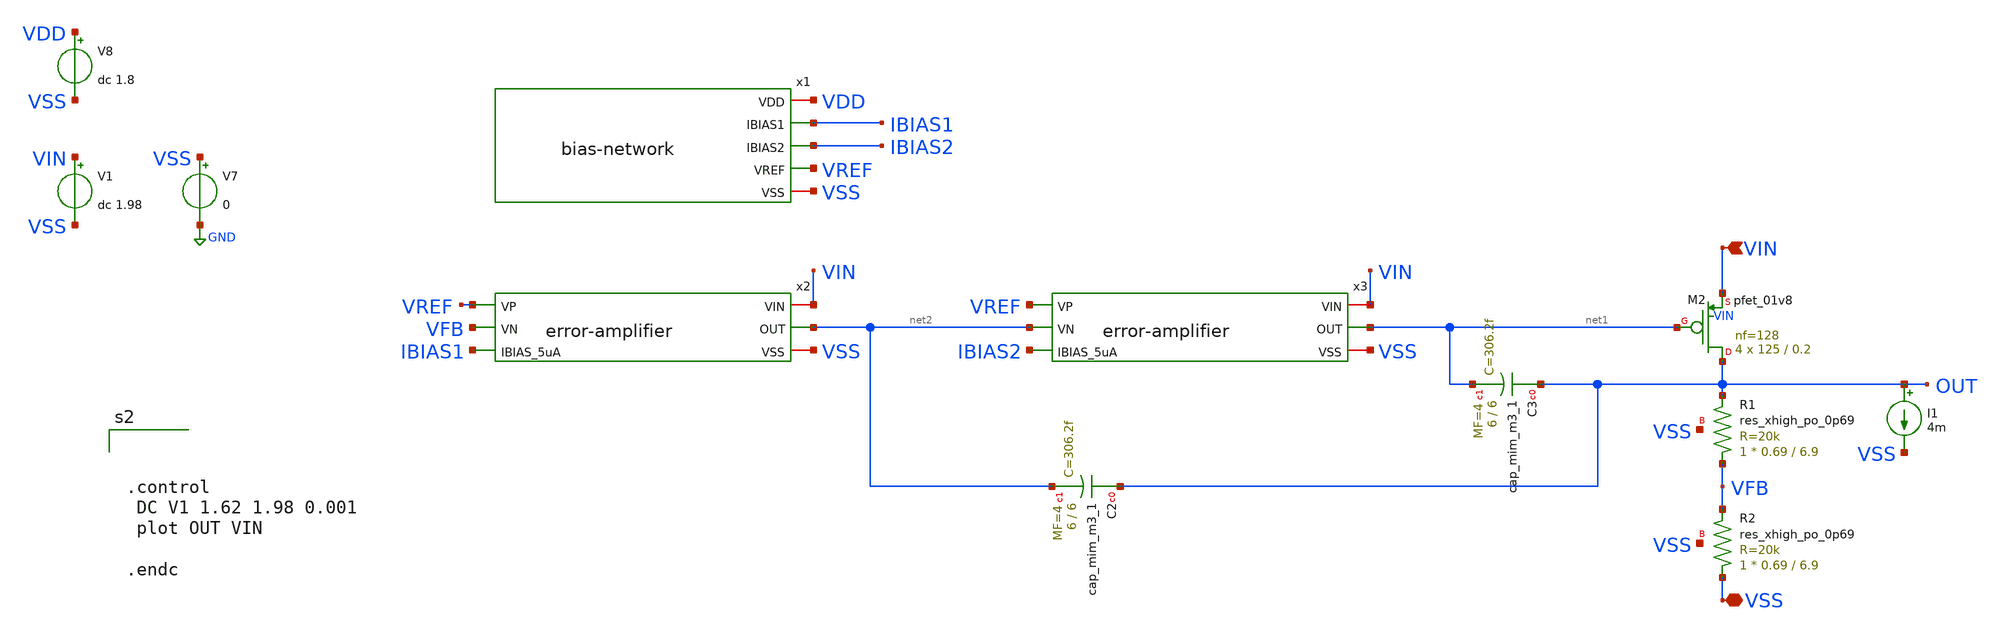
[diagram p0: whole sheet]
** sch_path: xschem/ldo_andriansyah/testbench/load-line-regulation.sch
**.subckt load-line-regulation VIN VSS
*.ipin VIN
*.iopin VSS
V7 VSS GND 0
V1 VIN VSS dc 1.98
I1 OUT VSS 4m
XC2 OUT net2 sky130_fd_pr__cap_mim_m3_1 W=6 L=6 MF=4 m=4
XC3 OUT net1 sky130_fd_pr__cap_mim_m3_1 W=6 L=6 MF=4 m=4
XR1 VFB OUT VSS sky130_fd_pr__res_xhigh_po_0p69 L=6.9 mult=1 m=1
XR2 VSS VFB VSS sky130_fd_pr__res_xhigh_po_0p69 L=6.9 mult=1 m=1
XM2 OUT net1 VIN VIN sky130_fd_pr__pfet_01v8 L=0.2 W=125 nf=128 ad='int((nf+1)/2) * W/nf * 0.29' as='int((nf+2)/2) * W/nf * 0.29'
+ pd='2*int((nf+1)/2) * (W/nf + 0.29)' ps='2*int((nf+2)/2) * (W/nf + 0.29)' nrd='0.29 / W' nrs='0.29 / W'
+ sa=0 sb=0 sd=0 mult=4 m=4
x1 VDD IBIAS1 IBIAS2 VREF VSS bias-network
V8 VDD VSS dc 1.8
x2 VIN VREF VFB IBIAS1 net2 VSS error-amplifier
x3 VIN VREF net2 IBIAS2 net1 VSS error-amplifier
**** begin user architecture code

** opencircuitdesign pdks install
.lib $::SKYWATER_MODELS/sky130.lib.spice tt





.control
 DC V1 1.62 1.98 0.001
 plot OUT VIN

.endc




**** end user architecture code
**.ends

* expanding   symbol:
*+  /foss/designs/2026/tt_sky26b_ldo_andriansyah/xschem/bias-net/schematics/bias-network.sym # of pins=5
** sym_path: xschem/bias-net/schematics/bias-network.sym
** sch_path: xschem/bias-net/schematics/bias-network.sch
.subckt bias-network VDD IBIAS1 IBIAS2 VREF VSS
*.iopin VDD
*.iopin VSS
*.opin IBIAS1
*.opin IBIAS2
*.opin VREF
XM2 VREF VREF VSS VSS sky130_fd_pr__nfet_01v8 L=2 W=3 nf=4 ad='int((nf+1)/2) * W/nf * 0.29' as='int((nf+2)/2) * W/nf * 0.29'
+ pd='2*int((nf+1)/2) * (W/nf + 0.29)' ps='2*int((nf+2)/2) * (W/nf + 0.29)' nrd='0.29 / W' nrs='0.29 / W'
+ sa=0 sb=0 sd=0 mult=2 m=2
XR1 VREF net1 VSS sky130_fd_pr__res_xhigh_po_0p69 L=6.9 mult=1 m=1
XR2 net2 net1 VSS sky130_fd_pr__res_xhigh_po_0p69 L=6.9 mult=1 m=1
XR3 net2 net3 VSS sky130_fd_pr__res_xhigh_po_0p69 L=6.9 mult=1 m=1
XR4 net4 net3 VSS sky130_fd_pr__res_xhigh_po_0p69 L=6.9 mult=1 m=1
XR5 net4 net5 VSS sky130_fd_pr__res_xhigh_po_0p69 L=6.9 mult=1 m=1
XR6 net9 net10 VSS sky130_fd_pr__res_xhigh_po_0p69 L=6.9 mult=1 m=1
XR7 net9 net8 VSS sky130_fd_pr__res_xhigh_po_0p69 L=6.9 mult=1 m=1
XR8 net7 net8 VSS sky130_fd_pr__res_xhigh_po_0p69 L=6.9 mult=1 m=1
XR9 net7 net6 VSS sky130_fd_pr__res_xhigh_po_0p69 L=6.9 mult=1 m=1
XR10 net5 net6 VSS sky130_fd_pr__res_xhigh_po_0p69 L=6.9 mult=1 m=1
XM1 IBIAS1 VREF VSS VSS sky130_fd_pr__nfet_01v8 L=2 W=3 nf=4 ad='int((nf+1)/2) * W/nf * 0.29' as='int((nf+2)/2) * W/nf * 0.29'
+ pd='2*int((nf+1)/2) * (W/nf + 0.29)' ps='2*int((nf+2)/2) * (W/nf + 0.29)' nrd='0.29 / W' nrs='0.29 / W'
+ sa=0 sb=0 sd=0 mult=2 m=2
XM3 IBIAS2 VREF VSS VSS sky130_fd_pr__nfet_01v8 L=2 W=3 nf=4 ad='int((nf+1)/2) * W/nf * 0.29' as='int((nf+2)/2) * W/nf * 0.29'
+ pd='2*int((nf+1)/2) * (W/nf + 0.29)' ps='2*int((nf+2)/2) * (W/nf + 0.29)' nrd='0.29 / W' nrs='0.29 / W'
+ sa=0 sb=0 sd=0 mult=2 m=2
XR11 net10 net11 VSS sky130_fd_pr__res_xhigh_po_0p69 L=6.9 mult=1 m=1
XR12 net12 net11 VSS sky130_fd_pr__res_xhigh_po_0p69 L=6.9 mult=1 m=1
XR13 net12 net13 VSS sky130_fd_pr__res_xhigh_po_0p69 L=6.9 mult=1 m=1
XR14 net14 net13 VSS sky130_fd_pr__res_xhigh_po_0p69 L=6.9 mult=1 m=1
XR15 net14 net15 VSS sky130_fd_pr__res_xhigh_po_0p69 L=6.9 mult=1 m=1
XR16 net19 VDD VSS sky130_fd_pr__res_xhigh_po_0p69 L=6.9 mult=1 m=1
XR17 net19 net18 VSS sky130_fd_pr__res_xhigh_po_0p69 L=6.9 mult=1 m=1
XR18 net17 net18 VSS sky130_fd_pr__res_xhigh_po_0p69 L=6.9 mult=1 m=1
XR19 net17 net16 VSS sky130_fd_pr__res_xhigh_po_0p69 L=6.9 mult=1 m=1
XR20 net15 net16 VSS sky130_fd_pr__res_xhigh_po_0p69 L=6.9 mult=1 m=1
XR21 VSS VSS VSS sky130_fd_pr__res_xhigh_po_0p69 L=6.9 mult=1 m=1
XR22 VSS VSS VSS sky130_fd_pr__res_xhigh_po_0p69 L=6.9 mult=1 m=1
.ends


* expanding   symbol:
*+  /foss/designs/2026/tt_sky26b_ldo_andriansyah/xschem/error-amplifier/error-amplifier.sym # of pins=6
** sym_path: xschem/error-amplifier/error-amplifier.sym
** sch_path: xschem/error-amplifier/error-amplifier.sch
.subckt error-amplifier VIN VP VN IBIAS_5uA OUT VSS
*.ipin IBIAS_5uA
*.ipin VN
*.ipin VP
*.iopin VIN
*.iopin VSS
*.opin OUT
XM1 net2 net2 VSS VSS sky130_fd_pr__nfet_01v8 L=0.6 W=4.2 nf=4 ad='int((nf+1)/2) * W/nf * 0.29' as='int((nf+2)/2) * W/nf * 0.29'
+ pd='2*int((nf+1)/2) * (W/nf + 0.29)' ps='2*int((nf+2)/2) * (W/nf + 0.29)' nrd='0.29 / W' nrs='0.29 / W'
+ sa=0 sb=0 sd=0 mult=1 m=1
XM2 OUT net2 VSS VSS sky130_fd_pr__nfet_01v8 L=0.6 W=4.2 nf=4 ad='int((nf+1)/2) * W/nf * 0.29' as='int((nf+2)/2) * W/nf * 0.29'
+ pd='2*int((nf+1)/2) * (W/nf + 0.29)' ps='2*int((nf+2)/2) * (W/nf + 0.29)' nrd='0.29 / W' nrs='0.29 / W'
+ sa=0 sb=0 sd=0 mult=1 m=1
XM3 net2 VN net1 VDD sky130_fd_pr__pfet_01v8 L=0.6 W=14 nf=4 ad='int((nf+1)/2) * W/nf * 0.29' as='int((nf+2)/2) * W/nf * 0.29'
+ pd='2*int((nf+1)/2) * (W/nf + 0.29)' ps='2*int((nf+2)/2) * (W/nf + 0.29)' nrd='0.29 / W' nrs='0.29 / W'
+ sa=0 sb=0 sd=0 mult=2 m=2
XM4 OUT VP net1 VDD sky130_fd_pr__pfet_01v8 L=0.6 W=14 nf=4 ad='int((nf+1)/2) * W/nf * 0.29' as='int((nf+2)/2) * W/nf * 0.29'
+ pd='2*int((nf+1)/2) * (W/nf + 0.29)' ps='2*int((nf+2)/2) * (W/nf + 0.29)' nrd='0.29 / W' nrs='0.29 / W'
+ sa=0 sb=0 sd=0 mult=2 m=2
XM5 net1 IBIAS_5uA VIN VIN sky130_fd_pr__pfet_01v8 L=0.6 W=6.6 nf=4 ad='int((nf+1)/2) * W/nf * 0.29'
+ as='int((nf+2)/2) * W/nf * 0.29' pd='2*int((nf+1)/2) * (W/nf + 0.29)' ps='2*int((nf+2)/2) * (W/nf + 0.29)'
+ nrd='0.29 / W' nrs='0.29 / W' sa=0 sb=0 sd=0 mult=1 m=1
XM6 IBIAS_5uA IBIAS_5uA VIN VIN sky130_fd_pr__pfet_01v8 L=0.6 W=6.6 nf=4 ad='int((nf+1)/2) * W/nf * 0.29'
+ as='int((nf+2)/2) * W/nf * 0.29' pd='2*int((nf+1)/2) * (W/nf + 0.29)' ps='2*int((nf+2)/2) * (W/nf + 0.29)'
+ nrd='0.29 / W' nrs='0.29 / W' sa=0 sb=0 sd=0 mult=1 m=1
.ends

.GLOBAL GND
.end
